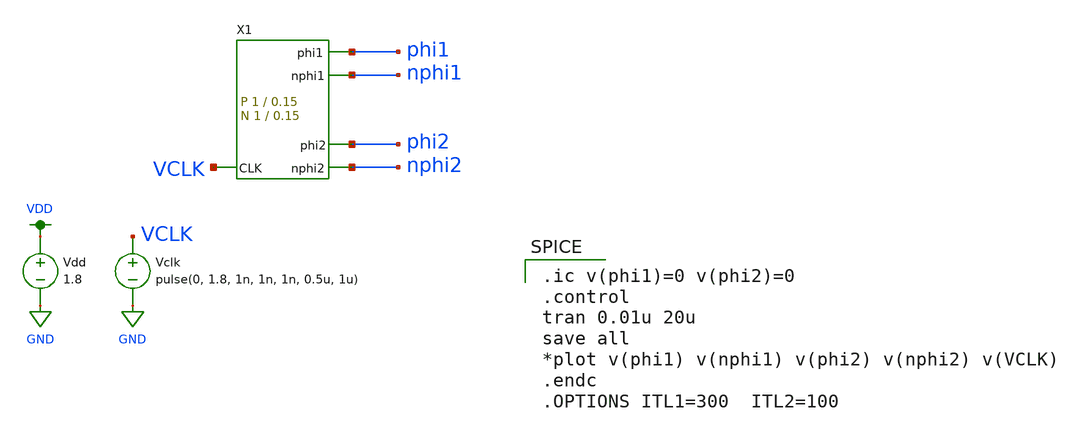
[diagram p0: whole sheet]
** sch_path: schematic/test/clk_gen_test.sch
**.subckt clk_gen_test
X1 phi1 phi2 VCLK nphi1 nphi2 clk_gen Wp=1 Lp=0.15 WW=1 LL=0.15
Vclk VCLK GND pulse(0, 1.8, 1n, 1n, 1n, 0.5u, 1u)
Vdd VDD GND 1.8
**** begin user architecture code

.option wnflag=1
.param MC_SWITCH=0.0
.lib ~/skywater/skywater-pdk/libraries/sky130_fd_pr_ngspice/latest/models/sky130.lib.spice tt


.ic v(phi1)=0 v(phi2)=0
.control
tran 0.01u 20u
save all
*plot v(phi1) v(nphi1) v(phi2) v(nphi2) v(VCLK)
.endc
.OPTIONS ITL1=300  ITL2=100

**** end user architecture code
**.ends

* expanding   symbol:  /home/madvlsi/Documents/MADVLSI-Final_Project/schematic/clk_gen.sym # of
*+ pins=5
** sym_path: schematic/clk_gen.sym
** sch_path: schematic/clk_gen.sch
.subckt clk_gen phi1 phi2 CLK nphi1 nphi2  Wp=1 Lp=0.15 WW=1 LL=0.15
*.opin phi1
*.opin nphi1
*.opin nphi2
*.opin phi2
*.ipin CLK
X3 CLK net1 VDD GND inverter
X4 phi2 nphi2 VDD GND inverter
X5 phi1 nphi1 VDD GND inverter
X1 phi1 phi2 net1 nor2 Wp={Wp} Lp={Lp} WW={WW} LL={LL}
X2 CLK phi1 phi2 nor2 Wp={Wp} Lp={Lp} WW={WW} LL={LL}
.ends


* expanding   symbol:  /home/madvlsi/Documents/MADVLSI-Final_Project/schematic/inverter.sym # of
*+ pins=4
** sym_path: schematic/inverter.sym
** sch_path: schematic/inverter.sch
.subckt inverter A Y VP VN
*.opin Y
*.ipin A
*.iopin VP
*.iopin VN
XM3 Y A VP VDD sky130_fd_pr__pfet_01v8 L={Lp} W={Wp} nf=1 ad='int((nf+1)/2) * W/nf * 0.29' as='int((nf+2)/2) * W/nf * 0.29'
+ pd='2*int((nf+1)/2) * (W/nf + 0.29)' ps='2*int((nf+2)/2) * (W/nf + 0.29)' nrd='0.29 / W' nrs='0.29 / W'
+ sa=0 sb=0 sd=0 mult=1 m=1
XM4 Y A VP VDD sky130_fd_pr__pfet_01v8 L={Lp} W={Wp} nf=1 ad='int((nf+1)/2) * W/nf * 0.29' as='int((nf+2)/2) * W/nf * 0.29'
+ pd='2*int((nf+1)/2) * (W/nf + 0.29)' ps='2*int((nf+2)/2) * (W/nf + 0.29)' nrd='0.29 / W' nrs='0.29 / W'
+ sa=0 sb=0 sd=0 mult=1 m=1
XM5 Y A VN GND sky130_fd_pr__nfet_01v8 L={Lp} W={Wp} nf=1 ad='int((nf+1)/2) * W/nf * 0.29' as='int((nf+2)/2) * W/nf * 0.29'
+ pd='2*int((nf+1)/2) * (W/nf + 0.29)' ps='2*int((nf+2)/2) * (W/nf + 0.29)' nrd='0.29 / W' nrs='0.29 / W'
+ sa=0 sb=0 sd=0 mult=1 m=1
.ends


* expanding   symbol:  /home/madvlsi/Documents/MADVLSI-Final_Project/schematic/nor2.sym # of pins=3
** sym_path: schematic/nor2.sym
** sch_path: schematic/nor2.sch
.subckt nor2 A Y B  Wp=1 Lp=0.15 WW=1 LL=0.15
*.ipin A
*.ipin B
*.opin Y
XM1 Y A GND GND sky130_fd_pr__nfet_01v8 L={LL} W={WW} nf=1 ad='int((nf+1)/2) * W/nf * 0.29' as='int((nf+2)/2) * W/nf * 0.29'
+ pd='2*int((nf+1)/2) * (W/nf + 0.29)' ps='2*int((nf+2)/2) * (W/nf + 0.29)' nrd='0.29 / W' nrs='0.29 / W'
+ sa=0 sb=0 sd=0 mult=1 m=1
XM2 Y A net1 VDD sky130_fd_pr__pfet_01v8 L={Lp} W={Wp} nf=1 ad='int((nf+1)/2) * W/nf * 0.29' as='int((nf+2)/2) * W/nf * 0.29'
+ pd='2*int((nf+1)/2) * (W/nf + 0.29)' ps='2*int((nf+2)/2) * (W/nf + 0.29)' nrd='0.29 / W' nrs='0.29 / W'
+ sa=0 sb=0 sd=0 mult=1 m=1
XM3 net1 B VDD VDD sky130_fd_pr__pfet_01v8 L={Lp} W={Wp} nf=1 ad='int((nf+1)/2) * W/nf * 0.29' as='int((nf+2)/2) * W/nf * 0.29'
+ pd='2*int((nf+1)/2) * (W/nf + 0.29)' ps='2*int((nf+2)/2) * (W/nf + 0.29)' nrd='0.29 / W' nrs='0.29 / W'
+ sa=0 sb=0 sd=0 mult=1 m=1
XM4 GND B Y GND sky130_fd_pr__nfet_01v8 L={LL} W={WW} nf=1 ad='int((nf+1)/2) * W/nf * 0.29' as='int((nf+2)/2) * W/nf * 0.29'
+ pd='2*int((nf+1)/2) * (W/nf + 0.29)' ps='2*int((nf+2)/2) * (W/nf + 0.29)' nrd='0.29 / W' nrs='0.29 / W'
+ sa=0 sb=0 sd=0 mult=1 m=1
.ends

.GLOBAL GND
.GLOBAL VDD
.end
